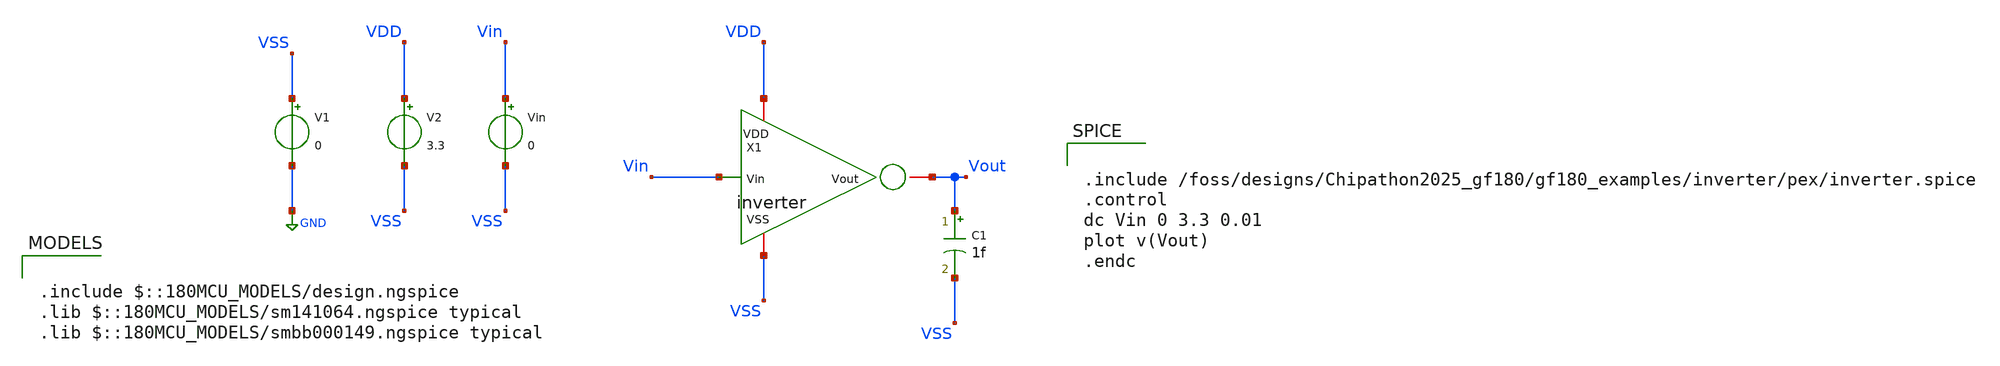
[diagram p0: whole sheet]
** sch_path: gf180_examples/inverter/pex/inverter_tb_none_ext.sch
**.subckt inverter_tb_none_ext
C1 Vout VSS 1f m=1
V1 VSS GND 0
V2 VDD VSS 3.3
Vin Vin VSS 0
X1 Vin VDD VSS Vout inverter
**** begin user architecture code

.include $::180MCU_MODELS/design.ngspice
.lib $::180MCU_MODELS/sm141064.ngspice typical
.lib $::180MCU_MODELS/smbb000149.ngspice typical



.include /foss/designs/Chipathon2025_gf180/gf180_examples/inverter/pex/inverter.spice
.control
dc Vin 0 3.3 0.01
plot v(Vout)
.endc


**** end user architecture code
**.ends
.GLOBAL GND
.end
